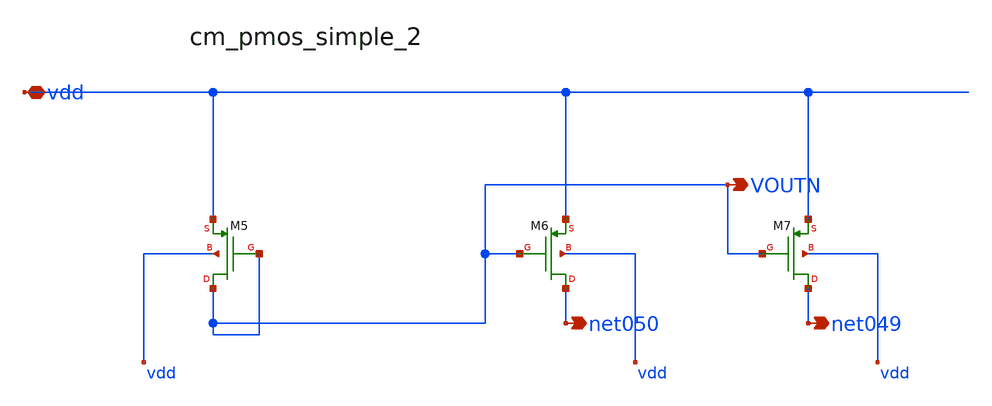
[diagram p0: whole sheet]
** sch_path: analog-db/raw/amp_015_sau_cfcc/hier/blocks/cm_pmos_simple_2.sch
**.subckt cm_pmos_simple_2 vdd VOUTN net050 net049
*.iopin vdd
*.opin VOUTN
*.opin net050
*.opin net049
XM5 VOUTN VOUTN vdd vdd sg13_lv_pmos w=x_dut_xm5_w l=x_dut_xm5_l ng=1 m=x_dut_xm5_m
XM6 net050 VOUTN vdd vdd sg13_lv_pmos w=x_dut_xm6_w l=x_dut_xm6_l ng=1 m=x_dut_xm6_m
XM7 net049 VOUTN vdd vdd sg13_lv_pmos w=x_dut_xm7_w l=x_dut_xm7_l ng=1 m=x_dut_xm7_m
**.ends
.end
